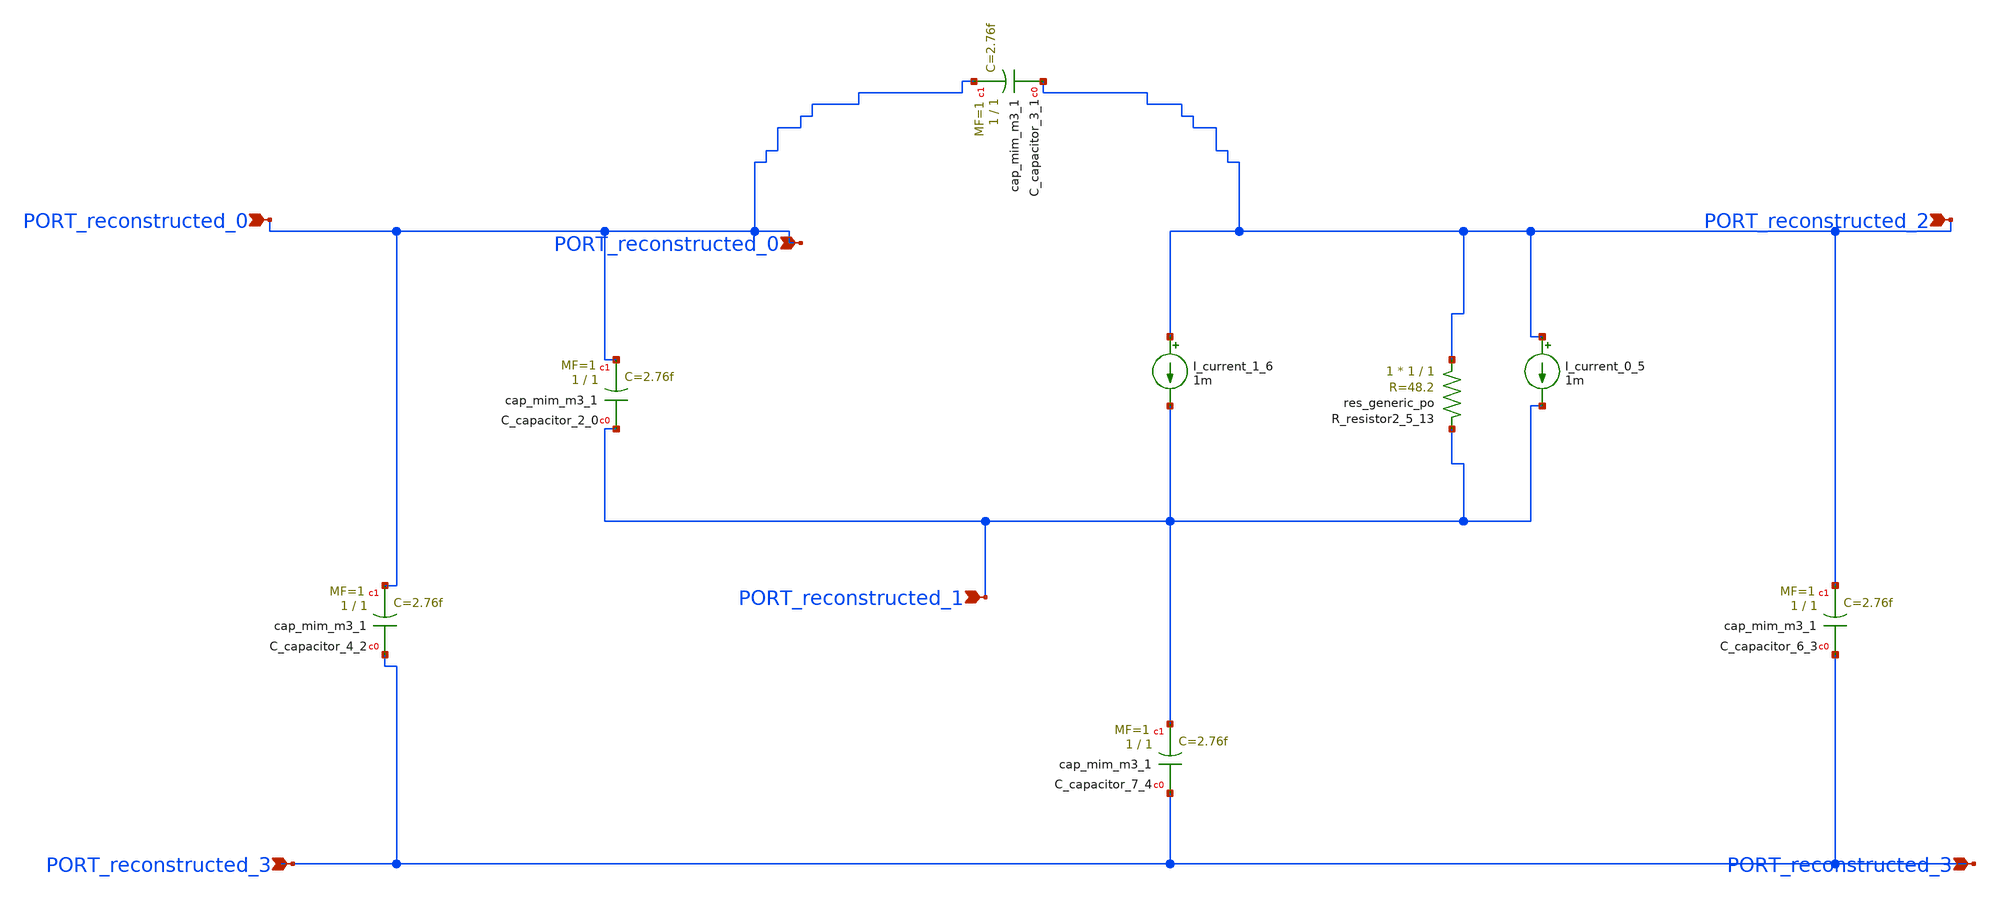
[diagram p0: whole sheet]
** sch_path: schematics/AMSNet/21.sch
**.subckt 21 PORT_reconstructed_1 PORT_reconstructed_3 PORT_reconstructed_3 PORT_reconstructed_0
*+ PORT_reconstructed_0 PORT_reconstructed_2
*.ipin PORT_reconstructed_1
*.ipin PORT_reconstructed_3
*.ipin PORT_reconstructed_3
*.ipin PORT_reconstructed_0
*.ipin PORT_reconstructed_0
*.ipin PORT_reconstructed_2
XC_capacitor_2_0 PORT_reconstructed_1 PORT_reconstructed_0 sky130_fd_pr__cap_mim_m3_1 W=1 L=1 MF=1
+ m=1
XC_capacitor_3_1 PORT_reconstructed_2 PORT_reconstructed_0 sky130_fd_pr__cap_mim_m3_1 W=1 L=1 MF=1
+ m=1
XC_capacitor_4_2 PORT_reconstructed_3 PORT_reconstructed_0 sky130_fd_pr__cap_mim_m3_1 W=1 L=1 MF=1
+ m=1
XC_capacitor_6_3 PORT_reconstructed_3 PORT_reconstructed_2 sky130_fd_pr__cap_mim_m3_1 W=1 L=1 MF=1
+ m=1
XC_capacitor_7_4 PORT_reconstructed_3 PORT_reconstructed_1 sky130_fd_pr__cap_mim_m3_1 W=1 L=1 MF=1
+ m=1
I_current_0_5 PORT_reconstructed_2 PORT_reconstructed_1 1m
I_current_1_6 PORT_reconstructed_2 PORT_reconstructed_1 1m
XR_resistor2_5_13 PORT_reconstructed_2 PORT_reconstructed_1 sky130_fd_pr__res_generic_po W=1 L=1 m=1
**.ends
.end
